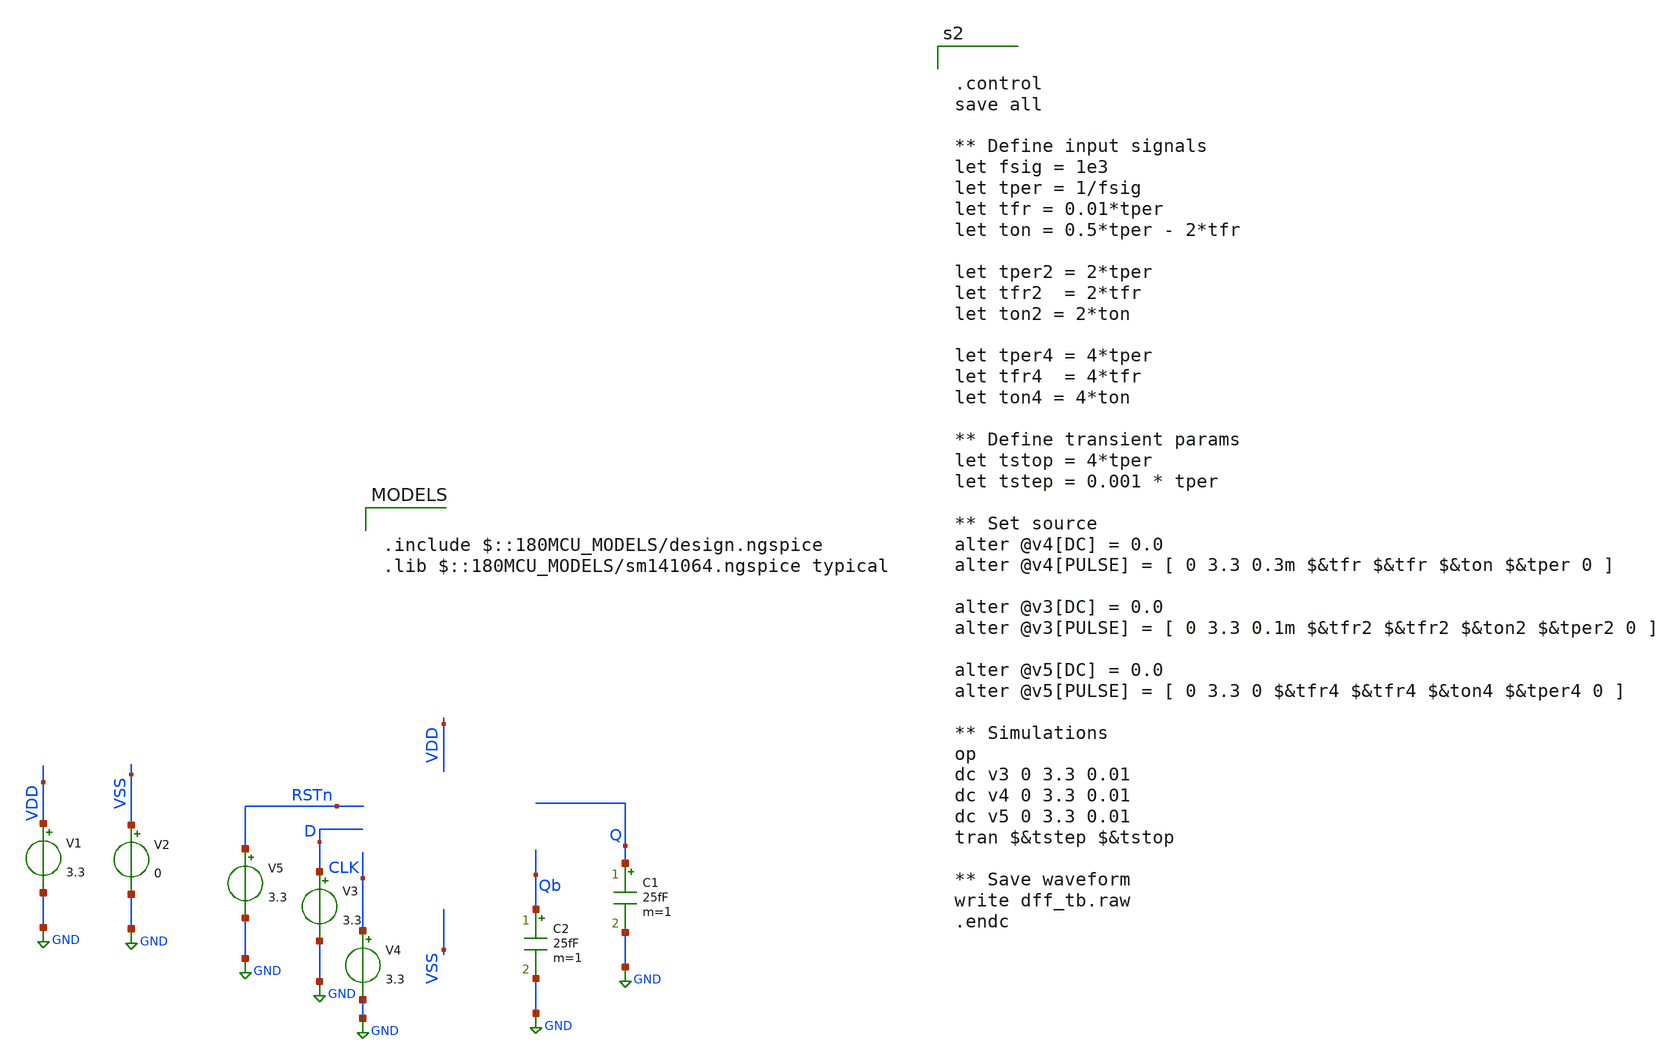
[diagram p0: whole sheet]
** sch_path: dff_postpex_tb.sch
**.subckt dff_postpex_tb
V1 VDD GND 3.3
V2 VSS GND 0
V3 D GND 3.3
C1 Q GND 25fF m=1
V4 CLK GND 3.3
C2 Qb GND 25fF m=1
V5 RSTn GND 3.3
**** begin user architecture code

.include $::180MCU_MODELS/design.ngspice
.lib $::180MCU_MODELS/sm141064.ngspice typical



.subckt dff_flat CHECK RSTN VDD CLK VSS D Q Qb
X0 a_n249_n4912# a_n1374_n6642# CHECK.t0 VSS.t1 nfet_03v3 ad=0.2646p pd=2.1u as=0.2646p ps=2.1u
+ w=0.42u l=0.28u
X1 VSS.t5 a_n359_n5759.t3 Q.t0 VSS.t4 nfet_03v3 ad=0.2646p pd=2.1u as=0.2646p ps=2.1u w=0.42u
+ l=0.28u
X2 a_n359_n5759.t2 a_n249_n4912# VDD.t21 VDD.t20 pfet_03v3 ad=0.1092p pd=0.94u as=0.2822p ps=2.18u
+ w=0.42u l=0.28u
X3 VDD.t19 RSTN.t0 a_881_n5758# VDD.t18 pfet_03v3 ad=0.2822p pd=2.18u as=0.1092p ps=0.94u w=0.42u
+ l=0.28u
X4 VDD.t3 a_n1374_n6642# a_1067_n6116# VDD.t2 pfet_03v3 ad=0.2822p pd=2.18u as=0.1092p ps=0.94u
+ w=0.42u l=0.28u
X5 a_2281_n4424# D.t0 a_1056_n4015# VSS.t10 nfet_03v3 ad=0.1092p pd=0.94u as=0.2646p ps=2.1u w=0.42u
+ l=0.28u
X6 VSS.t9 CLK.t0 a_n1342_n5730# VSS.t8 nfet_03v3 ad=0.2646p pd=2.1u as=0.2646p ps=2.1u w=0.42u
+ l=0.28u
X7 a_2280_n3998# D.t1 a_1056_n4015# VDD.t15 pfet_03v3 ad=0.1092p pd=0.94u as=0.2822p ps=2.18u
+ w=0.42u l=0.28u
X8 VDD.t17 CLK.t1 a_n1342_n5730# VDD.t16 pfet_03v3 ad=0.2822p pd=2.18u as=0.2822p ps=2.18u w=0.42u
+ l=0.28u
X9 VSS.t20 a_n1342_n5730# a_n1374_n6642# VSS.t19 nfet_03v3 ad=0.2667p pd=2.11u as=0.2625p ps=2.09u
+ w=0.42u l=0.28u
X10 a_1059_n5756# CHECK.t4 a_881_n5758# VSS.t25 nfet_03v3 ad=0.1092p pd=0.94u as=0.2646p ps=2.1u
+ w=0.42u l=0.28u
X11 VSS.t3 a_1056_n4015# CHECK.t2 VSS.t2 nfet_03v3 ad=0.2646p pd=2.1u as=0.2646p ps=2.1u w=0.42u
+ l=0.28u
X12 VSS.t18 a_n1342_n5730# a_1068_n6542# VSS.t17 nfet_03v3 ad=0.2646p pd=2.1u as=0.1092p ps=0.94u
+ w=0.42u l=0.28u
X13 VSS.t7 a_n912_n3722# Qb.t0 VSS.t6 nfet_03v3 ad=0.2646p pd=2.1u as=0.2646p ps=2.1u w=0.42u
+ l=0.28u
X14 VSS.t13 RSTN.t1 a_n181_n5757# VSS.t12 nfet_03v3 ad=0.2646p pd=2.1u as=0.1092p ps=0.94u w=0.42u
+ l=0.28u
X15 VDD.t14 a_n359_n5759.t4 Q.t1 VDD.t13 pfet_03v3 ad=0.2822p pd=2.18u as=0.2822p ps=2.18u w=0.42u
+ l=0.28u
X16 a_n249_n4912# a_n1342_n5730# CHECK.t3 VDD.t25 pfet_03v3 ad=0.2822p pd=2.18u as=0.2822p ps=2.18u
+ w=0.42u l=0.28u
X17 VSS.t22 a_n359_n5759.t5 a_n912_n3722# VSS.t21 nfet_03v3 ad=0.2646p pd=2.1u as=0.2646p ps=2.1u
+ w=0.42u l=0.28u
X18 VDD.t24 a_n1342_n5730# a_n1374_n6642# VDD.t23 pfet_03v3 ad=0.2822p pd=2.18u as=0.2822p ps=2.18u
+ w=0.42u l=0.28u
X19 a_881_n5758# a_n1374_n6642# a_1056_n4015# VSS.t0 nfet_03v3 ad=0.2646p pd=2.1u as=0.2646p ps=2.1u
+ w=0.42u l=0.28u
X20 VDD.t9 a_n912_n3722# Qb.t1 VDD.t8 pfet_03v3 ad=0.2822p pd=2.18u as=0.2822p ps=2.18u w=0.42u
+ l=0.28u
X21 VSS.t16 a_n1342_n5730# a_2281_n4424# VSS.t15 nfet_03v3 ad=0.2646p pd=2.1u as=0.1092p ps=0.94u
+ w=0.42u l=0.28u
X22 VDD.t5 RSTN.t2 a_n359_n5759.t0 VDD.t4 pfet_03v3 ad=0.2822p pd=2.18u as=0.1092p ps=0.94u w=0.42u
+ l=0.28u
X23 VDD.t1 a_n1374_n6642# a_2280_n3998# VDD.t0 pfet_03v3 ad=0.2822p pd=2.18u as=0.1092p ps=0.94u
+ w=0.42u l=0.28u
X24 a_1067_n6116# a_n359_n5759.t6 a_n249_n4912# VDD.t12 pfet_03v3 ad=0.1092p pd=0.94u as=0.2822p
+ ps=2.18u w=0.42u l=0.28u
X25 a_881_n5758# CHECK.t5 VDD.t27 VDD.t26 pfet_03v3 ad=0.1092p pd=0.94u as=0.2822p ps=2.18u w=0.42u
+ l=0.28u
X26 VSS.t24 RSTN.t3 a_1059_n5756# VSS.t23 nfet_03v3 ad=0.2646p pd=2.1u as=0.1092p ps=0.94u w=0.42u
+ l=0.28u
X27 VDD.t7 a_1056_n4015# CHECK.t1 VDD.t6 pfet_03v3 ad=0.2822p pd=2.18u as=0.2822p ps=2.18u w=0.42u
+ l=0.28u
X28 a_881_n5758# a_n1342_n5730# a_1056_n4015# VDD.t22 pfet_03v3 ad=0.2822p pd=2.18u as=0.2822p
+ ps=2.18u w=0.42u l=0.28u
X29 a_1068_n6542# a_n359_n5759.t7 a_n249_n4912# VSS.t11 nfet_03v3 ad=0.1092p pd=0.94u as=0.2646p
+ ps=2.1u w=0.42u l=0.28u
X30 a_n181_n5757# a_n249_n4912# a_n359_n5759.t1 VSS.t14 nfet_03v3 ad=0.1092p pd=0.94u as=0.2646p
+ ps=2.1u w=0.42u l=0.28u
X31 VDD.t11 a_n359_n5759.t8 a_n912_n3722# VDD.t10 pfet_03v3 ad=0.2822p pd=2.18u as=0.2822p ps=2.18u
+ w=0.42u l=0.28u
R0 CHECK.n0 CHECK.t5 72.3487
R1 CHECK.n0 CHECK.t4 16.9469
R2 CHECK.n1 CHECK.t0 12.9962
R3 CHECK.n3 CHECK.t2 12.3135
R4 CHECK CHECK.t1 12.2112
R5 CHECK.n1 CHECK.t3 12.0263
R6 CHECK.n2 CHECK.n0 9.90023
R7 CHECK CHECK.n3 0.449361
R8 CHECK.n2 CHECK.n1 0.39464
R9 CHECK.n3 CHECK.n2 0.156576
R10 VSS.n23 VSS.n16 749278
R11 VSS.n16 VSS.t10 91327.6
R12 VSS.n5 VSS.n3 64653.5
R13 VSS.n50 VSS.n3 47027.8
R14 VSS.n13 VSS.n8 11150.5
R15 VSS.t6 VSS.n46 10656.3
R16 VSS.n46 VSS.n45 9310.54
R17 VSS.n6 VSS.n3 9172.39
R18 VSS.n17 VSS.n8 8859.18
R19 VSS.n46 VSS.n7 7710.44
R20 VSS.n43 VSS.n9 6769.51
R21 VSS.n35 VSS.n34 6625.47
R22 VSS.n45 VSS.n8 5874.35
R23 VSS.t19 VSS.n49 4464.13
R24 VSS.n13 VSS.n11 4354.26
R25 VSS.n30 VSS.n10 4226.8
R26 VSS.n29 VSS.n11 4102.23
R27 VSS.n45 VSS.n44 3676.98
R28 VSS.n24 VSS.n23 3564.92
R29 VSS.n44 VSS.t0 2894.81
R30 VSS.n47 VSS.n7 2588.74
R31 VSS.t4 VSS.n3 2474.65
R32 VSS.n49 VSS.n48 2224.45
R33 VSS.n49 VSS.t8 1774.36
R34 VSS.n48 VSS.n6 1755.92
R35 VSS.n22 VSS.n21 1702.15
R36 VSS.t2 VSS.n24 1689.9
R37 VSS.n24 VSS.n10 1589.78
R38 VSS.t8 VSS.n5 1493.57
R39 VSS.t15 VSS.n15 1430.46
R40 VSS.n25 VSS.t2 1413.04
R41 VSS.t25 VSS.n9 1360.03
R42 VSS.n21 VSS.t0 1205.49
R43 VSS.t21 VSS.n7 1196.19
R44 VSS.n48 VSS.n47 1177.13
R45 VSS.n18 VSS.t23 1172.44
R46 VSS.n23 VSS.n22 1095.11
R47 VSS.n25 VSS.n11 1090.87
R48 VSS.n36 VSS.t12 1070.49
R49 VSS.n34 VSS.t11 1055.67
R50 VSS.n42 VSS.t21 992.063
R51 VSS.n30 VSS.t1 940.115
R52 VSS.n50 VSS.t19 920.712
R53 VSS.t10 VSS.t15 915.494
R54 VSS.n18 VSS.n10 900.433
R55 VSS.n34 VSS.n33 836.077
R56 VSS.n36 VSS.n35 822.135
R57 VSS.n32 VSS.n30 797.649
R58 VSS.t23 VSS.t25 750.361
R59 VSS.t12 VSS.t14 685.112
R60 VSS.n17 VSS.n16 674.74
R61 VSS.n38 VSS.n7 671.655
R62 VSS.n43 VSS.n42 615.08
R63 VSS.n33 VSS.t4 604.99
R64 VSS.t17 VSS.n32 576.241
R65 VSS.t1 VSS.n29 492.724
R66 VSS.n44 VSS.n43 472.2
R67 VSS.n15 VSS.n13 469.19
R68 VSS.t14 VSS.n6 466.733
R69 VSS.n47 VSS.t6 415.238
R70 VSS.t11 VSS.t17 368.795
R71 VSS.n35 VSS.n9 317.529
R72 VSS.n22 VSS.n17 57.864
R73 VSS.n21 VSS.n20 15.3475
R74 VSS.n51 VSS.t20 12.5437
R75 VSS.n37 VSS.t13 12.4687
R76 VSS.n31 VSS.t18 12.4687
R77 VSS.n19 VSS.t24 12.4687
R78 VSS.n26 VSS.t3 12.4687
R79 VSS.n41 VSS.t22 12.4687
R80 VSS.n4 VSS.t9 12.4687
R81 VSS.n1 VSS.t5 12.4687
R82 VSS.n38 VSS.t7 12.4687
R83 VSS.n14 VSS.t16 12.4675
R84 VSS.n29 VSS.n28 11.6695
R85 VSS.n15 VSS.n14 10.4017
R86 VSS.n19 VSS.n18 10.4005
R87 VSS.n26 VSS.n25 10.4005
R88 VSS.n5 VSS.n4 10.4005
R89 VSS.n33 VSS.n1 10.4005
R90 VSS.n51 VSS.n50 10.4005
R91 VSS.n42 VSS.n41 10.4005
R92 VSS.n32 VSS.n31 10.4005
R93 VSS.n37 VSS.n36 10.4005
R94 VSS.n31 VSS.n0 9.86036
R95 VSS.n28 VSS.n27 6.42418
R96 VSS.n20 VSS.n19 6.02652
R97 VSS.n39 VSS.n38 5.75457
R98 VSS.n39 VSS.n2 5.48837
R99 VSS.n41 VSS.n40 5.44665
R100 VSS.n40 VSS.n37 5.3877
R101 VSS.n27 VSS.n26 4.66984
R102 VSS.n14 VSS.n12 4.6547
R103 VSS.n20 VSS.n12 1.34731
R104 VSS.n40 VSS.n39 1.2245
R105 VSS.n27 VSS.n12 1.03428
R106 VSS.n52 VSS.n2 0.820259
R107 VSS VSS.n0 0.783577
R108 VSS.n28 VSS.n0 0.664346
R109 VSS.n53 VSS.n52 0.652808
R110 VSS VSS.n53 0.348192
R111 VSS.n4 VSS.n2 0.323682
R112 VSS.n53 VSS.n1 0.322765
R113 VSS.n52 VSS.n51 0.314599
R114 a_n359_n5759.t8 a_n359_n5759.t5 69.3505
R115 a_n359_n5759.t4 a_n359_n5759.t3 69.3505
R116 a_n359_n5759.t6 a_n359_n5759.t7 53.4469
R117 a_n359_n5759.n0 a_n359_n5759.t6 35.2609
R118 a_n359_n5759.n2 a_n359_n5759.t8 30.3133
R119 a_n359_n5759.n0 a_n359_n5759.t4 25.048
R120 a_n359_n5759.n1 a_n359_n5759.t1 12.3005
R121 a_n359_n5759.n3 a_n359_n5759.n2 5.78668
R122 a_n359_n5759.t0 a_n359_n5759.n3 4.33383
R123 a_n359_n5759.n3 a_n359_n5759.t2 4.33383
R124 a_n359_n5759.n1 a_n359_n5759.n0 0.519935
R125 a_n359_n5759.n2 a_n359_n5759.n1 0.494983
R126 Q Q.t0 12.6202
R127 Q Q.t1 12.341
R128 VDD.n8 VDD.t25 715.11
R129 VDD.n11 VDD.t22 714.49
R130 VDD.n18 VDD.t23 713.694
R131 VDD.n14 VDD.t8 713.688
R132 VDD.n17 VDD.t16 713.688
R133 VDD.n12 VDD.t4 713.688
R134 VDD.n16 VDD.t10 713.688
R135 VDD.n9 VDD.t0 713.688
R136 VDD.n6 VDD.t6 713.688
R137 VDD.n0 VDD.t18 713.688
R138 VDD.n3 VDD.t2 713.688
R139 VDD.n2 VDD.t13 713.688
R140 VDD.t4 VDD.t20 434.784
R141 VDD.t0 VDD.t15 434.784
R142 VDD.t18 VDD.t26 434.784
R143 VDD.t2 VDD.t12 434.784
R144 VDD.n0 VDD.t27 13.7623
R145 VDD.n13 VDD.t21 12.5331
R146 VDD.n17 VDD.t17 12.1992
R147 VDD.n16 VDD.t11 12.1992
R148 VDD.n6 VDD.t7 12.1992
R149 VDD.n3 VDD.t3 12.1992
R150 VDD.n2 VDD.t14 12.1992
R151 VDD.n14 VDD.t9 12.198
R152 VDD.n10 VDD.t1 12.1968
R153 VDD.n18 VDD.t24 12.192
R154 VDD.n12 VDD.t5 12.1422
R155 VDD.n1 VDD.t19 12.1411
R156 VDD.n19 VDD.n18 11.4596
R157 VDD.n16 VDD.n15 9.90617
R158 VDD.n4 VDD.n2 7.0573
R159 VDD.n7 VDD.n5 5.46986
R160 VDD.n5 VDD.n1 5.05424
R161 VDD.n4 VDD.n3 5.0066
R162 VDD.n20 VDD.n19 3.429
R163 VDD.n11 VDD.n10 1.6793
R164 VDD.n19 VDD.n17 1.5236
R165 VDD.n9 VDD.n8 1.27962
R166 VDD.n13 VDD.n12 1.1387
R167 VDD VDD.n11 0.864995
R168 VDD.n5 VDD.n4 0.845079
R169 VDD.n20 VDD.n16 0.527474
R170 VDD.n15 VDD.n14 0.516611
R171 VDD.n15 VDD.n13 0.457423
R172 VDD.n8 VDD.n7 0.351026
R173 VDD VDD.n20 0.00545413
R174 VDD.n10 VDD.n9 0.00286842
R175 VDD.n7 VDD.n6 0.00168421
R176 VDD.n1 VDD.n0 0.00153448
R177 RSTN.t0 RSTN.t3 89.2951
R178 RSTN.t2 RSTN.t1 89.2951
R179 RSTN.n0 RSTN.t2 44.9198
R180 RSTN.n0 RSTN.t0 24.9469
R181 RSTN RSTN.n0 0.00168421
R182 D.t1 D.t0 53.4469
R183 D D.t1 24.9505
R184 CLK.t1 CLK.t0 69.3505
R185 CLK CLK.t1 24.9517
R186 Qb Qb.t0 12.6395
R187 Qb Qb.t1 12.3217
C0 a_1056_n4015# CHECK 0.10365f
C1 a_n912_n3722# VDD 0.83176f
C2 a_881_n5758# a_n249_n4912# 0.19693f
C3 a_n1342_n5730# VDD 1.71536f
C4 a_n1374_n6642# a_n1342_n5730# 1.67868f
C5 a_1056_n4015# VDD 0.95856f
C6 a_881_n5758# a_n1342_n5730# 0.31376f
C7 a_n1374_n6642# a_1056_n4015# 0.2678f
C8 a_881_n5758# a_1056_n4015# 0.25267f
C9 RSTN a_n249_n4912# 0.28644f
C10 VDD D 0.18707f
C11 VDD CLK 0.28794f
C12 VDD Qb 0.10704f
C13 a_n1342_n5730# a_n249_n4912# 0.21283f
C14 VDD CHECK 0.76938f
C15 a_n1374_n6642# CHECK 0.22275f
C16 a_881_n5758# CHECK 0.35092f
C17 a_n1374_n6642# VDD 1.886f
C18 a_881_n5758# VDD 1.18904f
C19 a_881_n5758# a_n1374_n6642# 0.24946f
C20 RSTN CHECK 0.29193f
C21 RSTN VDD 0.80322f
C22 a_n249_n4912# CHECK 0.11019f
C23 VDD a_n249_n4912# 0.56511f
C24 a_n1374_n6642# a_n249_n4912# 0.23084f
C25 Q VSS 0.25589f
C26 CLK VSS 0.39888f
C27 CHECK VSS 1.33038f
C28 RSTN VSS 1.32962f
C29 D VSS 0.27844f
C30 Qb VSS 0.15428f
C31 VDD VSS 18.83505f
C32 a_n249_n4912# VSS 2.53842f
C33 a_881_n5758# VSS 0.89126f
C34 a_1056_n4015# VSS 1.26966f
C35 a_n1374_n6642# VSS 5.44569f
C36 a_n1342_n5730# VSS 6.88765f
C37 a_n912_n3722# VSS 0.62392f
C38 VDD.n8 VSS 0.11133f
C39 VDD.n11 VSS 0.13113f
C40 VDD.n19 VSS 0.21025f
C41 VDD.n20 VSS 0.10843f
C42 a_n359_n5759.t8 VSS 0.19196f
C43 a_n359_n5759.t6 VSS 0.11284f
C44 a_n359_n5759.n0 VSS 0.45569f
C45 a_n359_n5759.n1 VSS 0.14466f
C46 a_n359_n5759.n2 VSS 1.35777f
.ends

X0 CHECK RSTN VDD CLK VSS D Q Qb dff_flat




.control
save all

** Define input signals
let fsig = 1e3
let tper = 1/fsig
let tfr = 0.01*tper
let ton = 0.5*tper - 2*tfr

let tper2 = 2*tper
let tfr2  = 2*tfr
let ton2 = 2*ton

let tper4 = 4*tper
let tfr4  = 4*tfr
let ton4 = 4*ton

** Define transient params
let tstop = 4*tper
let tstep = 0.001 * tper

** Set source
alter @v4[DC] = 0.0
alter @v4[PULSE] = [ 0 3.3 0.3m $&tfr $&tfr $&ton $&tper 0 ]

alter @v3[DC] = 0.0
alter @v3[PULSE] = [ 0 3.3 0.1m $&tfr2 $&tfr2 $&ton2 $&tper2 0 ]

alter @v5[DC] = 0.0
alter @v5[PULSE] = [ 0 3.3 0 $&tfr4 $&tfr4 $&ton4 $&tper4 0 ]

** Simulations
op
dc v3 0 3.3 0.01
dc v4 0 3.3 0.01
dc v5 0 3.3 0.01
tran $&tstep $&tstop

** Save waveform
write dff_tb.raw
.endc


**** end user architecture code
**.ends
.GLOBAL GND
.end
